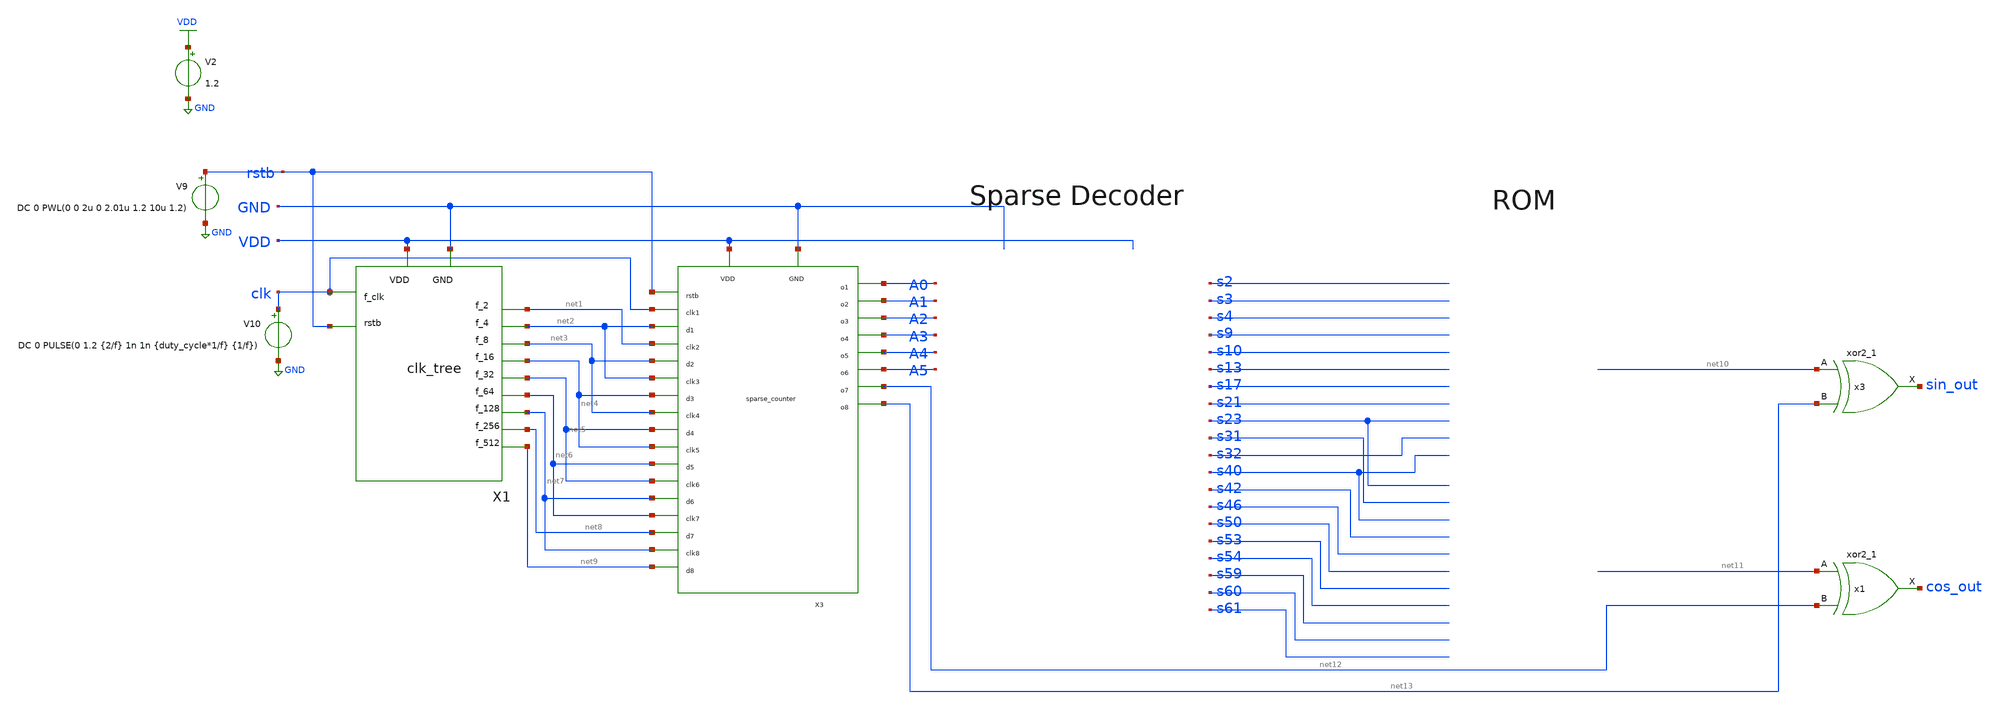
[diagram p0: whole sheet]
** sch_path: xschem/Sinusoid_generator/lo_gen.sch
**.subckt lo_gen
X1 rstb clk net1 net2 net3 net4 net5 net6 net7 net8 net9 VDD GND clk_tree
X3 VDD GND rstb clk net2 net1 net3 net2 net4 net3 net5 net4 net6 net5 net7 net6 net8 net7 net9 A0 A1
+ A2 A3 A4 A5 net12 net13 sparse_counter
x3 net10 net13 GND GND VDD VDD sin_out sky130_fd_sc_lp__xor2_1
x1 net11 net12 GND GND VDD VDD cos_out sky130_fd_sc_lp__xor2_1
V2 VDD GND 1.2
V9 rstb GND DC 0 PWL(0 0 2u 0 2.01u 1.2 10u 1.2)
V10 clk GND DC 0 PULSE(0 1.2 {2/f} 1n 1n {duty_cycle*1/f} {1/f})
**** begin user architecture code


.lib /home/sky/sky130A/libs.tech/ngspice/sky130.lib.spice tt
.include /home/sky/sky130A/libs.ref/sky130_fd_sc_lp/spice/sky130_fd_sc_lp.spice
.options abstol=1e-18 reltol=1e-4
.param f=2560k
.param duty_cycle=0.5
.tran {(1/100)*(1/f)} {256/f}
.save all


**** end user architecture code
**.ends

* expanding   symbol:  clk_tree/clk_tree.sym # of pins=13
** sym_path: xschem/clk_tree/clk_tree.sym
** sch_path: xschem/clk_tree/clk_tree.sch
.subckt clk_tree rstb f_clk f_2 f_4 f_8 f_16 f_32 f_64 f_128 f_256 f_512 VDD GND
*.ipin rstb
*.iopin VDD
*.iopin GND
*.opin f_2
*.opin f_4
*.opin f_8
*.opin f_16
*.opin f_32
*.opin f_64
*.opin f_128
*.opin f_256
*.opin f_512
*.ipin f_clk
x2 f_clk net1 rstb gnd gnd vdd vdd f_2 net1 sky130_fd_sc_lp__dfrbp_1
x4 f_2 net2 rstb gnd gnd vdd vdd f_4 net2 sky130_fd_sc_lp__dfrbp_1
x1 f_4 net3 rstb gnd gnd vdd vdd f_8 net3 sky130_fd_sc_lp__dfrbp_1
x6 f_8 net4 rstb gnd gnd vdd vdd f_16 net4 sky130_fd_sc_lp__dfrbp_1
x7 f_16 net5 rstb gnd gnd vdd vdd f_32 net5 sky130_fd_sc_lp__dfrbp_1
x8 f_32 net6 rstb gnd gnd vdd vdd f_64 net6 sky130_fd_sc_lp__dfrbp_1
x9 f_64 net7 rstb gnd gnd vdd vdd f_128 net7 sky130_fd_sc_lp__dfrbp_1
x14 f_128 net8 rstb gnd gnd vdd vdd f_256 net8 sky130_fd_sc_lp__dfrbp_1
x15 f_256 net9 rstb gnd gnd vdd vdd f_512 net9 sky130_fd_sc_lp__dfrbp_1
.ends


* expanding   symbol:  sparse_counter/sparse_counter.sym # of pins=27
** sym_path: xschem/sparse_counter/sparse_counter.sym
** sch_path: xschem/sparse_counter/sparse_counter.sch
.subckt sparse_counter VDD GND rstb clk1 d1 clk2 d2 clk3 d3 clk4 d4 clk5 d5 clk6 d6 clk7 d7 clk8 d8
+ o1 o2 o3 o4 o5 o6 o7 o8
*.iopin VDD
*.iopin GND
*.ipin rstb
*.ipin clk1
*.ipin d1
*.ipin clk2
*.ipin clk3
*.ipin clk4
*.ipin clk5
*.ipin clk6
*.ipin clk7
*.ipin clk8
*.ipin d2
*.ipin d3
*.ipin d4
*.ipin d5
*.ipin d6
*.ipin d7
*.ipin d8
*.opin o1
*.opin o2
*.opin o3
*.opin o4
*.opin o5
*.opin o6
*.opin o7
*.opin o8
x20 clk1 d1 rstb GND GND VDD VDD o1 sky130_fd_sc_lp__dfrtp_1
x3 clk2 d2 rstb GND GND VDD VDD o2 sky130_fd_sc_lp__dfrtp_1
x5 clk3 d3 rstb GND GND VDD VDD o3 sky130_fd_sc_lp__dfrtp_1
x10 clk4 d4 rstb GND GND VDD VDD o4 sky130_fd_sc_lp__dfrtp_1
x11 clk5 d5 rstb GND GND VDD VDD o5 sky130_fd_sc_lp__dfrtp_1
x12 clk6 d6 rstb GND GND VDD VDD o6 sky130_fd_sc_lp__dfrtp_1
x13 clk7 d7 rstb GND GND VDD VDD o7 sky130_fd_sc_lp__dfrtp_1
x16 clk8 d8 rstb GND GND VDD VDD o8 sky130_fd_sc_lp__dfrtp_1
.ends

.GLOBAL GND
.GLOBAL VDD
.end
